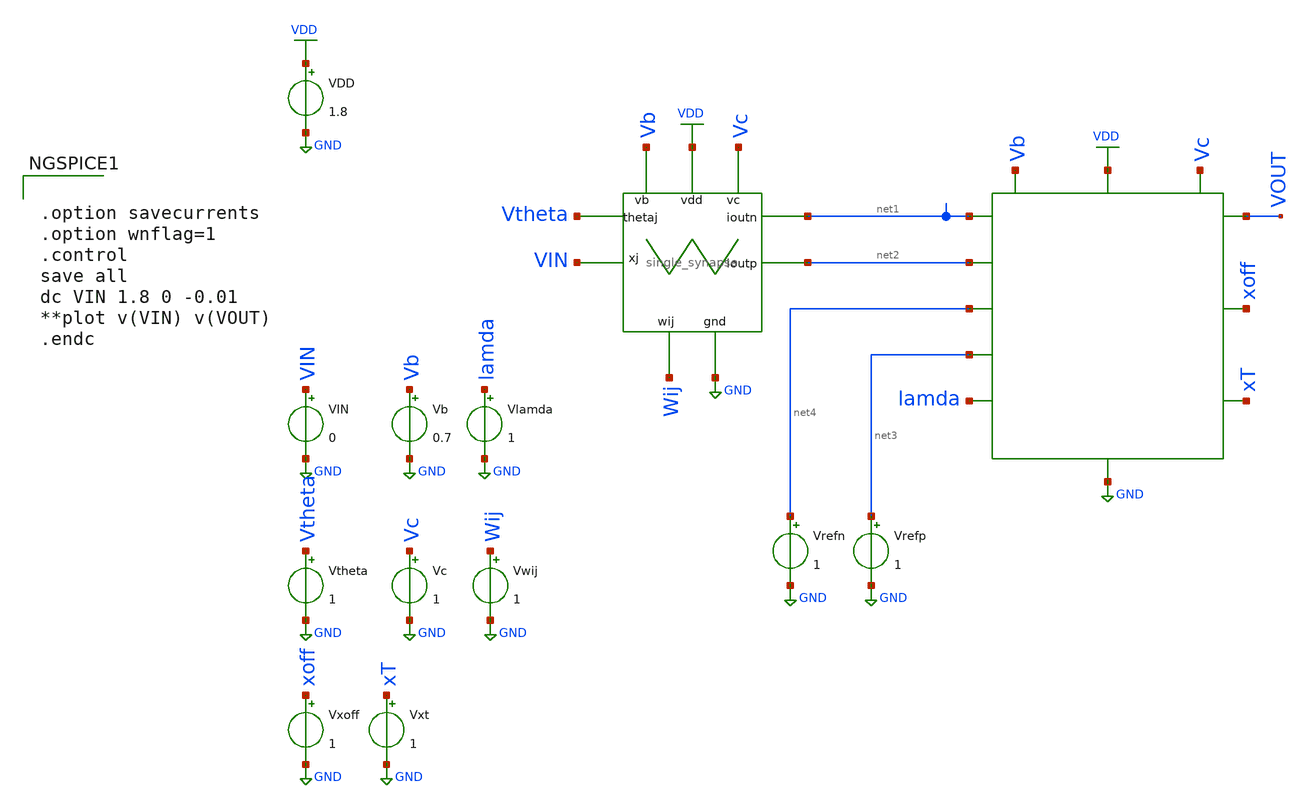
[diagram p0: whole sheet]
** sch_path: synapse_neuron_test.sch
**.subckt synapse_neuron_test
W1 Vtheta Vb VDD Vc VIN GND Wij net1 net2 single_synapse
VDD VDD GND 1.8
VIN VIN GND 0
Vb Vb GND 0.7
Vtheta Vtheta GND 1
Vc Vc GND 1
Vwij Wij GND 1
Vrefn net4 GND 1
Vrefp net3 GND 1
Vlamda lamda GND 1
Vxoff xoff GND 1
Vxt xT GND 1
**** begin user architecture code


.option savecurrents
.option wnflag=1
.control
save all
dc VIN 1.8 0 -0.01
**plot v(VIN) v(VOUT)
.endc



** opencircuitdesign pdks install
.lib $::SKYWATER_MODELS/sky130.lib.spice tt


**** end user architecture code
**.ends
.GLOBAL GND
.GLOBAL VDD
.end
